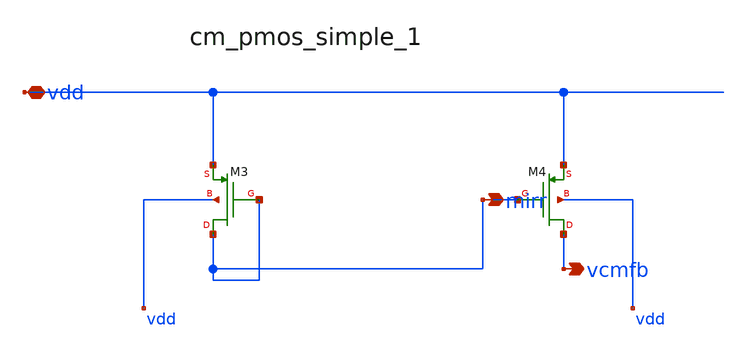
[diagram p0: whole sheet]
** sch_path: analog-db/raw/cmfb_003_5t_nmos_input/hier/blocks/cm_pmos_simple_1.sch
**.subckt cm_pmos_simple_1 vdd mirr vcmfb
*.iopin vdd
*.opin mirr
*.opin vcmfb
XM3 mirr mirr vdd vdd sg13_lv_pmos w=x_dut_xm3_w l=x_dut_xm3_l ng=1 m=x_dut_xm3_m
XM4 vcmfb mirr vdd vdd sg13_lv_pmos w=x_dut_xm4_w l=x_dut_xm4_l ng=1 m=x_dut_xm4_m
**.ends
.end
